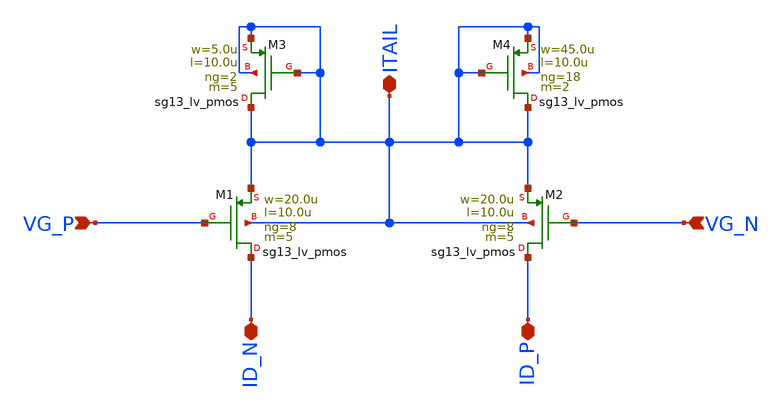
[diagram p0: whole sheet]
** sch_path: JKU_TC1/design_data/sfl-test-cells/xschem/diffpairs/dp_p_100u_10u.sch
**.subckt dp_p_100u_10u VG_P VG_N ITAIL ID_N ID_P
*.ipin VG_P
*.ipin VG_N
*.iopin ITAIL
*.iopin ID_N
*.iopin ID_P
XM1 ID_N VG_P ITAIL ITAIL sg13_lv_pmos w=20.0u l=10.0u ng=8 m=5 mm_ok=1
XM2 ID_P VG_N ITAIL ITAIL sg13_lv_pmos w=20.0u l=10.0u ng=8 m=5 mm_ok=1
XM3 ITAIL ITAIL ITAIL ITAIL sg13_lv_pmos w=5.0u l=10.0u ng=2 m=5 mm_ok=1
XM4 ITAIL ITAIL ITAIL ITAIL sg13_lv_pmos w=45.0u l=10.0u ng=18 m=2 mm_ok=1
**.ends
.end
